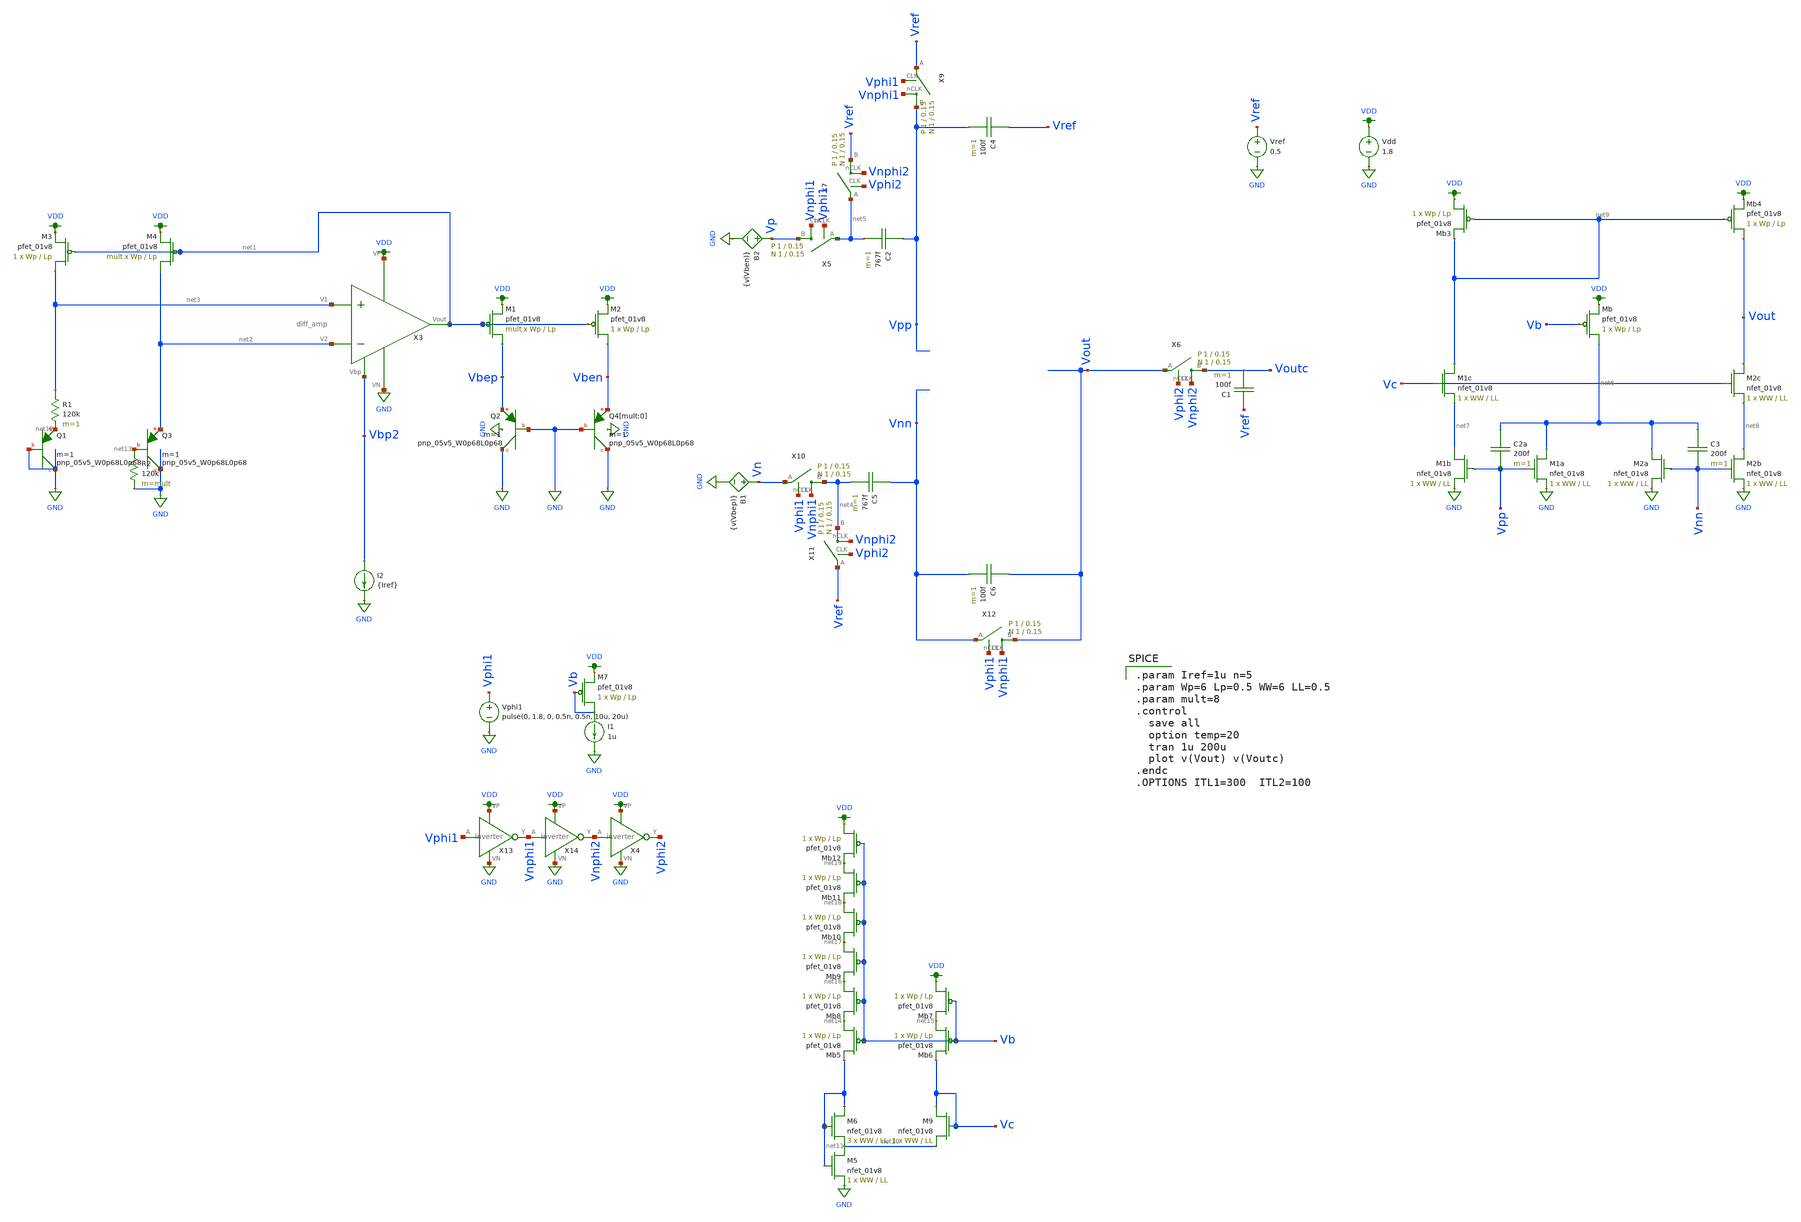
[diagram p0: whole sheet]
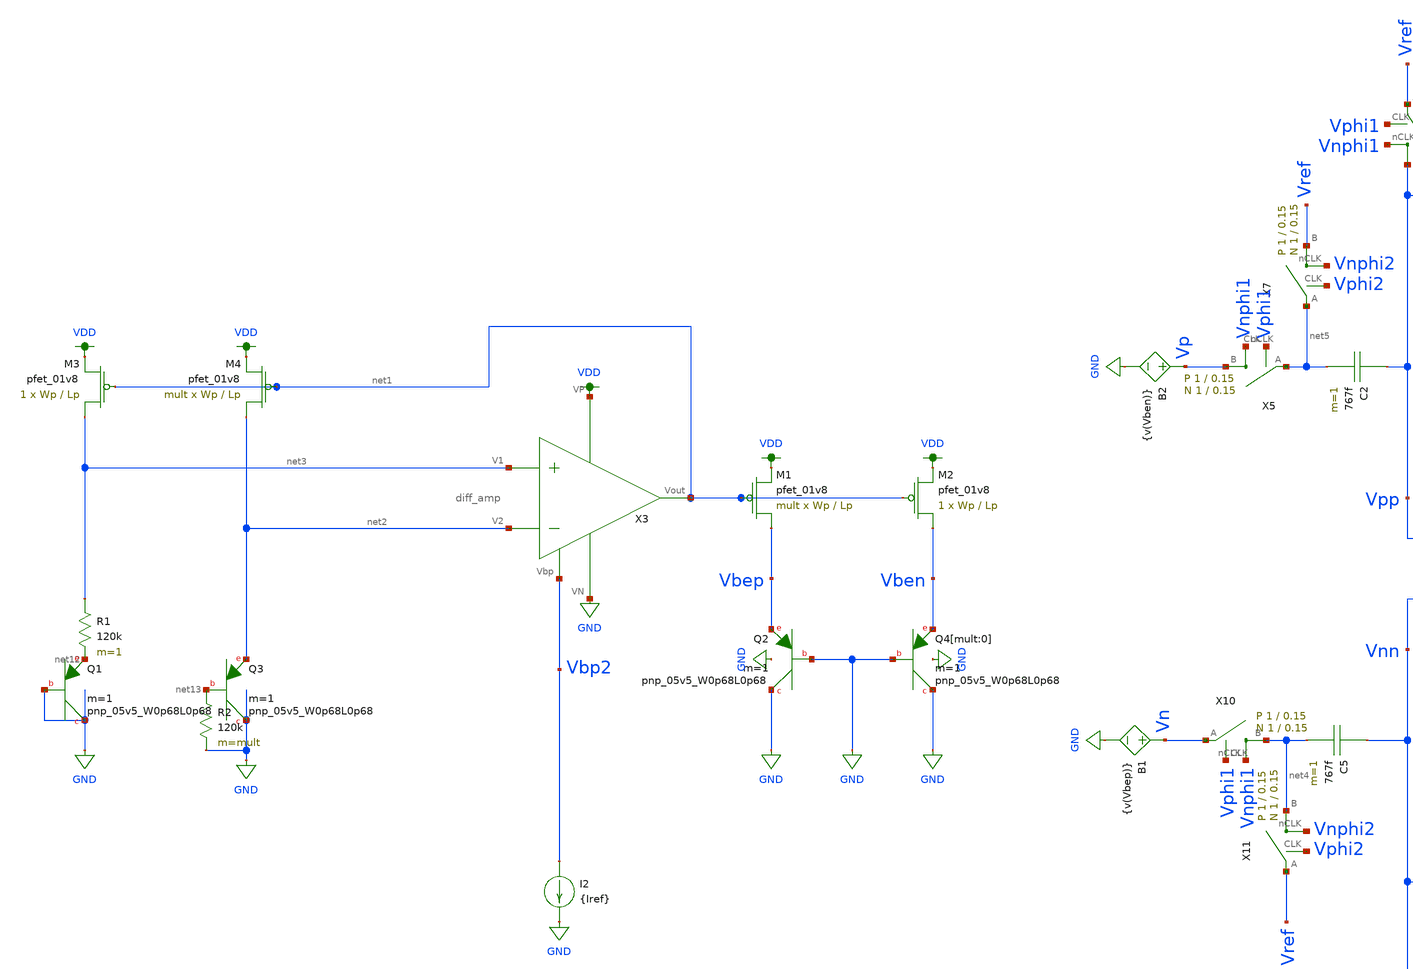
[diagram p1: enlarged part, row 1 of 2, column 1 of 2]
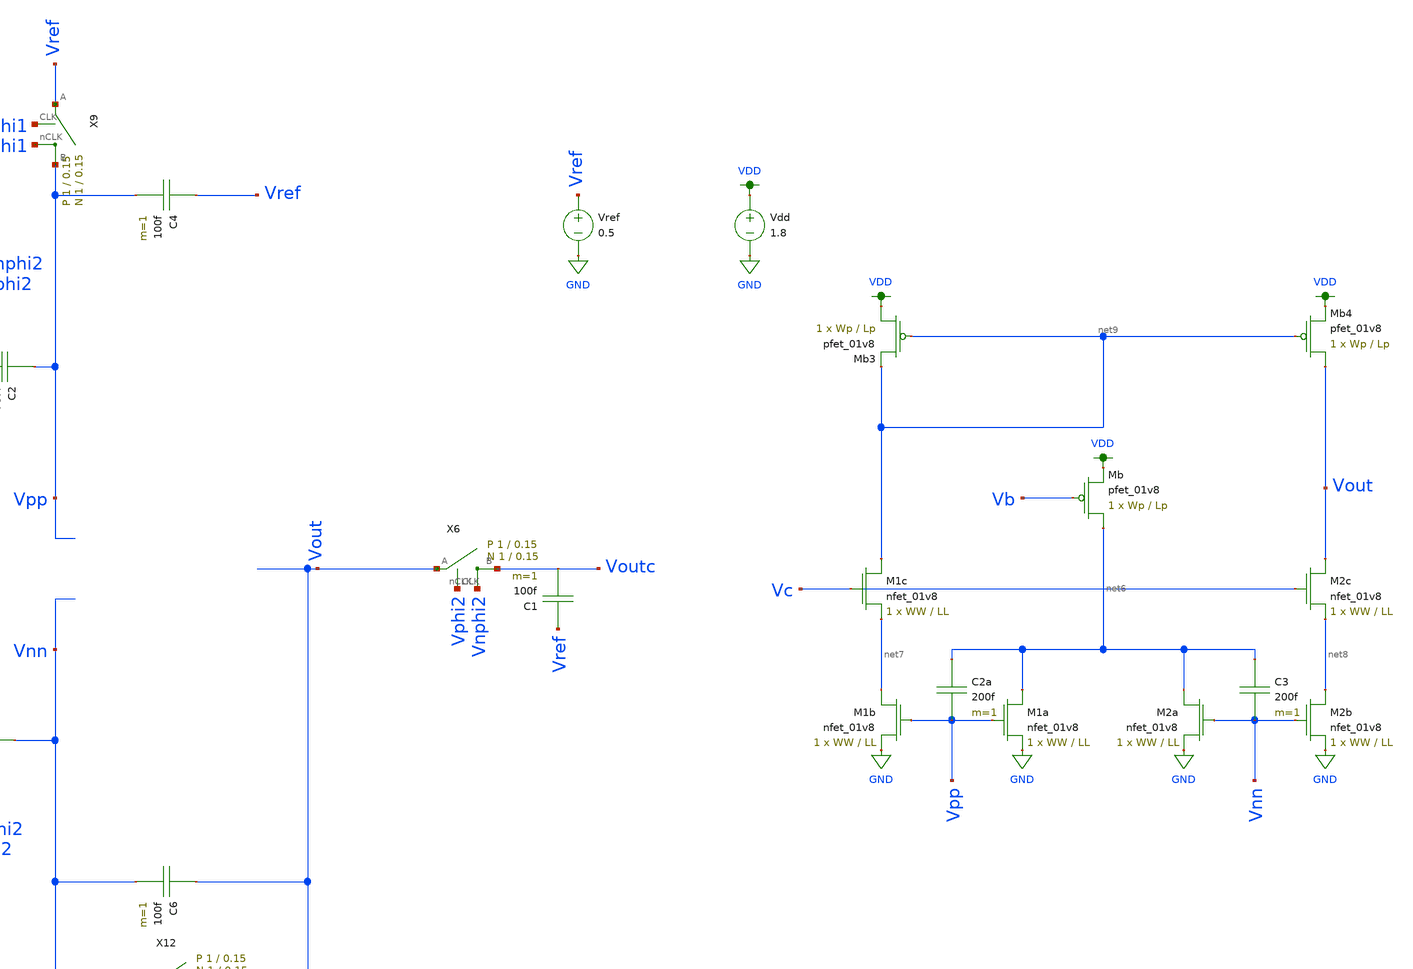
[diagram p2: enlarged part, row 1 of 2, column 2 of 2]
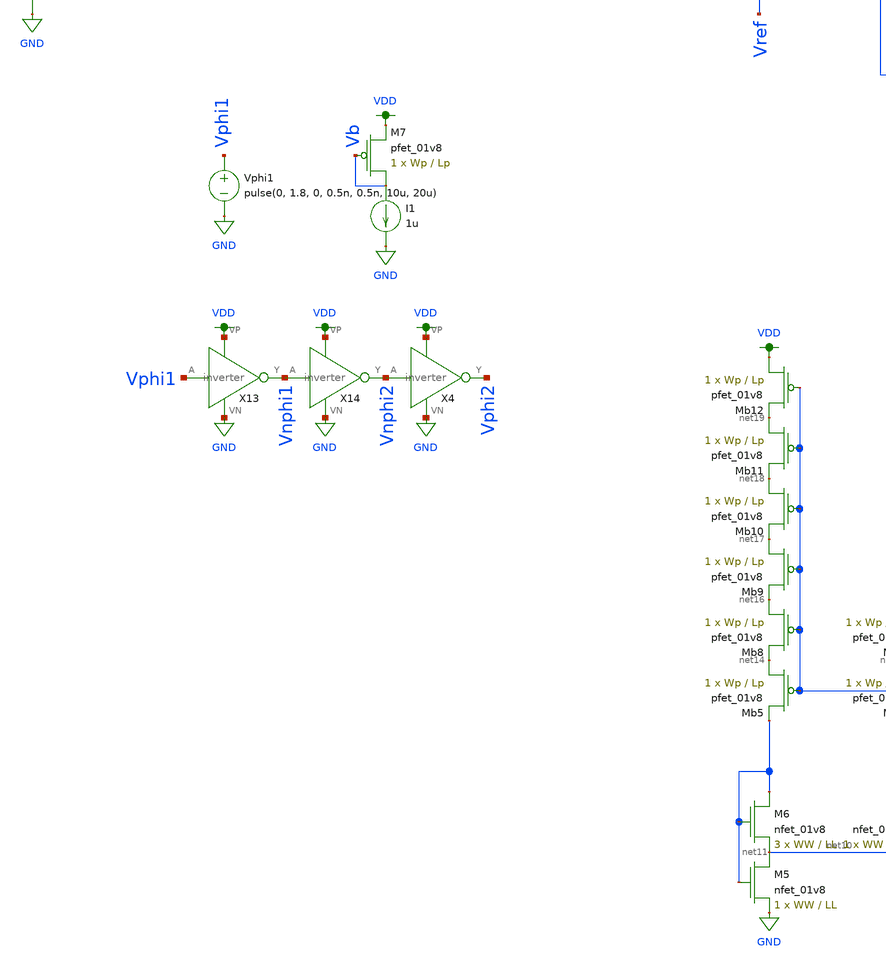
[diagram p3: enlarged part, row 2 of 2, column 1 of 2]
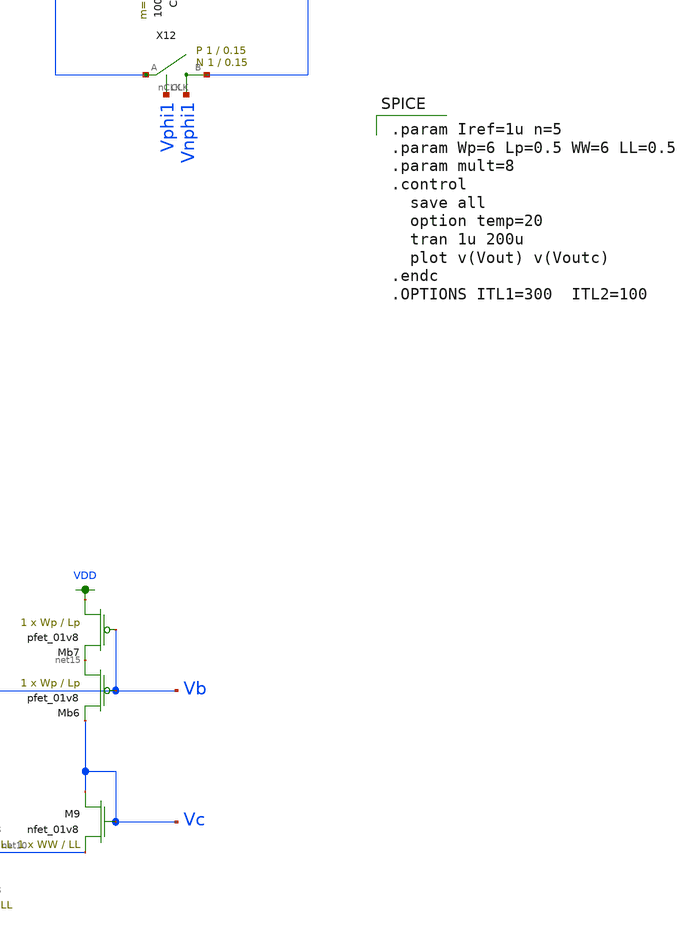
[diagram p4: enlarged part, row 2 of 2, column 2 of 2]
** sch_path: schematic/test/fg_bandgap.sch
**.subckt fg_bandgap
Vdd VDD GND 1.8
XQ2 GND GND Vbep sky130_fd_pr__pnp_05v5_W0p68L0p68 m=1
XM1 Vbep net1 VDD VDD sky130_fd_pr__pfet_01v8 L=Lp W=Wp nf=1 ad='int((nf+1)/2) * W/nf * 0.29' as='int((nf+2)/2) * W/nf * 0.29'
+ pd='2*int((nf+1)/2) * (W/nf + 0.29)' ps='2*int((nf+2)/2) * (W/nf + 0.29)' nrd='0.29 / W' nrs='0.29 / W'
+ sa=0 sb=0 sd=0 mult=mult m=mult
XM2 Vben net1 VDD VDD sky130_fd_pr__pfet_01v8 L=Lp W=Wp nf=1 ad='int((nf+1)/2) * W/nf * 0.29' as='int((nf+2)/2) * W/nf * 0.29'
+ pd='2*int((nf+1)/2) * (W/nf + 0.29)' ps='2*int((nf+2)/2) * (W/nf + 0.29)' nrd='0.29 / W' nrs='0.29 / W'
+ sa=0 sb=0 sd=0 mult=1 m=1
XQ4[mult:0] GND GND Vben sky130_fd_pr__pnp_05v5_W0p68L0p68 m=1
XQ1 GND GND net12 sky130_fd_pr__pnp_05v5_W0p68L0p68 m=1
XQ3 GND net13 net2 sky130_fd_pr__pnp_05v5_W0p68L0p68 m=1
R1 net3 net12 120k m=1
R2 net13 GND 120k m=mult
XM3 net3 net1 VDD VDD sky130_fd_pr__pfet_01v8 L=Lp W=Wp nf=1 ad='int((nf+1)/2) * W/nf * 0.29' as='int((nf+2)/2) * W/nf * 0.29'
+ pd='2*int((nf+1)/2) * (W/nf + 0.29)' ps='2*int((nf+2)/2) * (W/nf + 0.29)' nrd='0.29 / W' nrs='0.29 / W'
+ sa=0 sb=0 sd=0 mult=1 m=1
XM4 net2 net1 VDD VDD sky130_fd_pr__pfet_01v8 L=Lp W=Wp nf=1 ad='int((nf+1)/2) * W/nf * 0.29' as='int((nf+2)/2) * W/nf * 0.29'
+ pd='2*int((nf+1)/2) * (W/nf + 0.29)' ps='2*int((nf+2)/2) * (W/nf + 0.29)' nrd='0.29 / W' nrs='0.29 / W'
+ sa=0 sb=0 sd=0 mult=mult m=mult
X3 VDD Vbp2 net1 net3 net2 GND diff_amp
I2 Vbp2 GND {Iref}
C5 Vnn net4 767f m=1
C6 Vout Vnn 100f m=1
X10 net4 Vn Vphi1 Vnphi1 switch Wp=1 Lp=0.15 WW=1 LL=0.15
X11 net4 Vref Vphi2 Vnphi2 switch Wp=1 Lp=0.15 WW=1 LL=0.15
X12 Vout Vnn Vphi1 Vnphi1 switch Wp=1 Lp=0.15 WW=1 LL=0.15
C2 Vpp net5 767f m=1
C4 Vref Vpp 100f m=1
X5 Vp net5 Vphi1 Vnphi1 switch Wp=1 Lp=0.15 WW=1 LL=0.15
X7 Vref net5 Vphi2 Vnphi2 switch Wp=1 Lp=0.15 WW=1 LL=0.15
X9 Vpp Vref Vphi1 Vnphi1 switch Wp=1 Lp=0.15 WW=1 LL=0.15
Vref Vref GND 0.5
Vphi1 Vphi1 GND pulse(0, 1.8, 0, 0.5n, 0.5n, 10u, 20u)
X13 Vphi1 Vnphi1 VDD GND inverter
X14 Vnphi1 Vnphi2 VDD GND inverter
X4 Vnphi2 Vphi2 VDD GND inverter
B1 Vn GND V={v(Vbep)}
B2 Vp GND V={v(Vben)}
C1 Vref Voutc 100f m=1
X6 Voutc Vout Vphi2 Vnphi2 switch Wp=1 Lp=0.15 WW=1 LL=0.15
XM1a net6 Vpp GND GND sky130_fd_pr__nfet_01v8 L=LL W=WW nf=1 ad='int((nf+1)/2) * W/nf * 0.29' as='int((nf+2)/2) * W/nf * 0.29'
+ pd='2*int((nf+1)/2) * (W/nf + 0.29)' ps='2*int((nf+2)/2) * (W/nf + 0.29)' nrd='0.29 / W' nrs='0.29 / W'
+ sa=0 sb=0 sd=0 mult=1 m=1
XM1b net7 Vpp GND GND sky130_fd_pr__nfet_01v8 L=LL W=WW nf=1 ad='int((nf+1)/2) * W/nf * 0.29' as='int((nf+2)/2) * W/nf * 0.29'
+ pd='2*int((nf+1)/2) * (W/nf + 0.29)' ps='2*int((nf+2)/2) * (W/nf + 0.29)' nrd='0.29 / W' nrs='0.29 / W'
+ sa=0 sb=0 sd=0 mult=1 m=1
XM1c net9 Vc net7 GND sky130_fd_pr__nfet_01v8 L=LL W=WW nf=1 ad='int((nf+1)/2) * W/nf * 0.29' as='int((nf+2)/2) * W/nf * 0.29'
+ pd='2*int((nf+1)/2) * (W/nf + 0.29)' ps='2*int((nf+2)/2) * (W/nf + 0.29)' nrd='0.29 / W' nrs='0.29 / W'
+ sa=0 sb=0 sd=0 mult=1 m=1
XM2b net8 Vnn GND GND sky130_fd_pr__nfet_01v8 L=LL W=WW nf=1 ad='int((nf+1)/2) * W/nf * 0.29' as='int((nf+2)/2) * W/nf * 0.29'
+ pd='2*int((nf+1)/2) * (W/nf + 0.29)' ps='2*int((nf+2)/2) * (W/nf + 0.29)' nrd='0.29 / W' nrs='0.29 / W'
+ sa=0 sb=0 sd=0 mult=1 m=1
XM2a net6 Vnn GND GND sky130_fd_pr__nfet_01v8 L=LL W=WW nf=1 ad='int((nf+1)/2) * W/nf * 0.29' as='int((nf+2)/2) * W/nf * 0.29'
+ pd='2*int((nf+1)/2) * (W/nf + 0.29)' ps='2*int((nf+2)/2) * (W/nf + 0.29)' nrd='0.29 / W' nrs='0.29 / W'
+ sa=0 sb=0 sd=0 mult=1 m=1
XM2c Vout Vc net8 GND sky130_fd_pr__nfet_01v8 L=LL W=WW nf=1 ad='int((nf+1)/2) * W/nf * 0.29' as='int((nf+2)/2) * W/nf * 0.29'
+ pd='2*int((nf+1)/2) * (W/nf + 0.29)' ps='2*int((nf+2)/2) * (W/nf + 0.29)' nrd='0.29 / W' nrs='0.29 / W'
+ sa=0 sb=0 sd=0 mult=1 m=1
XMb net6 Vb VDD VDD sky130_fd_pr__pfet_01v8 L=Lp W=Wp nf=1 ad='int((nf+1)/2) * W/nf * 0.29' as='int((nf+2)/2) * W/nf * 0.29'
+ pd='2*int((nf+1)/2) * (W/nf + 0.29)' ps='2*int((nf+2)/2) * (W/nf + 0.29)' nrd='0.29 / W' nrs='0.29 / W'
+ sa=0 sb=0 sd=0 mult=1 m=1
C2a net6 Vpp 200f m=1
XMb3 VDD net9 net9 VDD sky130_fd_pr__pfet_01v8 L=Lp W=Wp nf=1 ad='int((nf+1)/2) * W/nf * 0.29' as='int((nf+2)/2) * W/nf * 0.29'
+ pd='2*int((nf+1)/2) * (W/nf + 0.29)' ps='2*int((nf+2)/2) * (W/nf + 0.29)' nrd='0.29 / W' nrs='0.29 / W'
+ sa=0 sb=0 sd=0 mult=1 m=1
XMb4 Vout net9 VDD VDD sky130_fd_pr__pfet_01v8 L=Lp W=Wp nf=1 ad='int((nf+1)/2) * W/nf * 0.29' as='int((nf+2)/2) * W/nf * 0.29'
+ pd='2*int((nf+1)/2) * (W/nf + 0.29)' ps='2*int((nf+2)/2) * (W/nf + 0.29)' nrd='0.29 / W' nrs='0.29 / W'
+ sa=0 sb=0 sd=0 mult=1 m=1
C3 net6 Vnn 200f m=1
XM5 net10 net11 GND GND sky130_fd_pr__nfet_01v8 L=LL W=WW nf=1 ad='int((nf+1)/2) * W/nf * 0.29' as='int((nf+2)/2) * W/nf * 0.29'
+ pd='2*int((nf+1)/2) * (W/nf + 0.29)' ps='2*int((nf+2)/2) * (W/nf + 0.29)' nrd='0.29 / W' nrs='0.29 / W'
+ sa=0 sb=0 sd=0 mult=1 m=1
XM6 net11 net11 net10 GND sky130_fd_pr__nfet_01v8 L=LL W=WW nf=1 ad='int((nf+1)/2) * W/nf * 0.29' as='int((nf+2)/2) * W/nf * 0.29'
+ pd='2*int((nf+1)/2) * (W/nf + 0.29)' ps='2*int((nf+2)/2) * (W/nf + 0.29)' nrd='0.29 / W' nrs='0.29 / W'
+ sa=0 sb=0 sd=0 mult=3 m=3
XM9 Vc Vc net10 GND sky130_fd_pr__nfet_01v8 L=LL W=WW nf=1 ad='int((nf+1)/2) * W/nf * 0.29' as='int((nf+2)/2) * W/nf * 0.29'
+ pd='2*int((nf+1)/2) * (W/nf + 0.29)' ps='2*int((nf+2)/2) * (W/nf + 0.29)' nrd='0.29 / W' nrs='0.29 / W'
+ sa=0 sb=0 sd=0 mult=1 m=1
XMb5 net14 Vb net11 VDD sky130_fd_pr__pfet_01v8 L=Lp W=Wp nf=1 ad='int((nf+1)/2) * W/nf * 0.29' as='int((nf+2)/2) * W/nf * 0.29'
+ pd='2*int((nf+1)/2) * (W/nf + 0.29)' ps='2*int((nf+2)/2) * (W/nf + 0.29)' nrd='0.29 / W' nrs='0.29 / W'
+ sa=0 sb=0 sd=0 mult=1 m=1
XMb6 net15 Vb Vc VDD sky130_fd_pr__pfet_01v8 L=Lp W=Wp nf=1 ad='int((nf+1)/2) * W/nf * 0.29' as='int((nf+2)/2) * W/nf * 0.29'
+ pd='2*int((nf+1)/2) * (W/nf + 0.29)' ps='2*int((nf+2)/2) * (W/nf + 0.29)' nrd='0.29 / W' nrs='0.29 / W'
+ sa=0 sb=0 sd=0 mult=1 m=1
XMb7 VDD Vb net15 VDD sky130_fd_pr__pfet_01v8 L=Lp W=Wp nf=1 ad='int((nf+1)/2) * W/nf * 0.29' as='int((nf+2)/2) * W/nf * 0.29'
+ pd='2*int((nf+1)/2) * (W/nf + 0.29)' ps='2*int((nf+2)/2) * (W/nf + 0.29)' nrd='0.29 / W' nrs='0.29 / W'
+ sa=0 sb=0 sd=0 mult=1 m=1
XMb8 net16 Vb net14 VDD sky130_fd_pr__pfet_01v8 L=Lp W=Wp nf=1 ad='int((nf+1)/2) * W/nf * 0.29' as='int((nf+2)/2) * W/nf * 0.29'
+ pd='2*int((nf+1)/2) * (W/nf + 0.29)' ps='2*int((nf+2)/2) * (W/nf + 0.29)' nrd='0.29 / W' nrs='0.29 / W'
+ sa=0 sb=0 sd=0 mult=1 m=1
XMb9 net17 Vb net16 VDD sky130_fd_pr__pfet_01v8 L=Lp W=Wp nf=1 ad='int((nf+1)/2) * W/nf * 0.29' as='int((nf+2)/2) * W/nf * 0.29'
+ pd='2*int((nf+1)/2) * (W/nf + 0.29)' ps='2*int((nf+2)/2) * (W/nf + 0.29)' nrd='0.29 / W' nrs='0.29 / W'
+ sa=0 sb=0 sd=0 mult=1 m=1
XMb10 net18 Vb net17 VDD sky130_fd_pr__pfet_01v8 L=Lp W=Wp nf=1 ad='int((nf+1)/2) * W/nf * 0.29' as='int((nf+2)/2) * W/nf * 0.29'
+ pd='2*int((nf+1)/2) * (W/nf + 0.29)' ps='2*int((nf+2)/2) * (W/nf + 0.29)' nrd='0.29 / W' nrs='0.29 / W'
+ sa=0 sb=0 sd=0 mult=1 m=1
XMb11 net19 Vb net18 VDD sky130_fd_pr__pfet_01v8 L=Lp W=Wp nf=1 ad='int((nf+1)/2) * W/nf * 0.29' as='int((nf+2)/2) * W/nf * 0.29'
+ pd='2*int((nf+1)/2) * (W/nf + 0.29)' ps='2*int((nf+2)/2) * (W/nf + 0.29)' nrd='0.29 / W' nrs='0.29 / W'
+ sa=0 sb=0 sd=0 mult=1 m=1
XMb12 VDD Vb net19 VDD sky130_fd_pr__pfet_01v8 L=Lp W=Wp nf=1 ad='int((nf+1)/2) * W/nf * 0.29' as='int((nf+2)/2) * W/nf * 0.29'
+ pd='2*int((nf+1)/2) * (W/nf + 0.29)' ps='2*int((nf+2)/2) * (W/nf + 0.29)' nrd='0.29 / W' nrs='0.29 / W'
+ sa=0 sb=0 sd=0 mult=1 m=1
XM7 Vb Vb VDD VDD sky130_fd_pr__pfet_01v8 L=Lp W=Wp nf=1 ad='int((nf+1)/2) * W/nf * 0.29' as='int((nf+2)/2) * W/nf * 0.29'
+ pd='2*int((nf+1)/2) * (W/nf + 0.29)' ps='2*int((nf+2)/2) * (W/nf + 0.29)' nrd='0.29 / W' nrs='0.29 / W'
+ sa=0 sb=0 sd=0 mult=1 m=1
I1 Vb GND 1u
**** begin user architecture code

.param Iref=1u n=5
.param Wp=6 Lp=0.5 WW=6 LL=0.5
.param mult=8
.control
  save all
  option temp=20
  tran 1u 200u
  plot v(Vout) v(Voutc)
.endc
.OPTIONS ITL1=300  ITL2=100


.option wnflag=1
.param MC_SWITCH=0.0
.lib /media/qdeng/526448C32060CF5C/skywater/skywater-pdk/libraries/sky130_fd_pr_ngspice/latest/models/sky130.lib.spice tt

**** end user architecture code
**.ends
.GLOBAL VDD
.GLOBAL GND
.end
